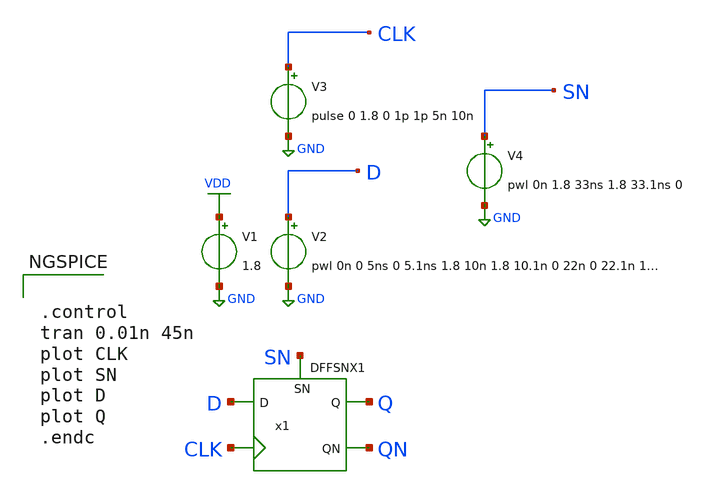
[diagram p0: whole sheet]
** sch_path: lib/xschem/test_DFFSNX1.sch
**.subckt test_DFFSNX1
V2 D GND pwl 0n 0 5ns 0 5.1ns 1.8 10n 1.8 10.1n 0 22n 0 22.1n 1.8 27n 1.8 27.1n 0 34n 0 34.1n 1.8
V1 VDD GND 1.8
V3 CLK GND pulse 0 1.8 0 1p 1p 5n 10n
V4 SN GND pwl 0n 1.8 33ns 1.8 33.1ns 0
x1 Q QN D CLK SN VDD GND DFFSNX1
**** begin user architecture code

.lib $::SKYWATER_MODELS/sky130.lib.spice tt


**** end user architecture code
**.ends

* expanding   symbol:  DFFSNX1.sym # of pins=5
** sym_path: DFFSNX1.sym
** sch_path: DFFSNX1.sch
.subckt DFFSNX1 Q QN D CLK SN VDD VSS
*.ipin D
*.opin QN
*.ipin SN
*.ipin CLK
*.opin Q
x1 net3 net1 SN net4 VDD VSS NAND3X1
x2 net4 net3 CLK VDD VSS NAND2X1
x3 net2 net1 CLK net4 VDD VSS NAND3X1
x4 net1 D net2 VDD VSS NAND2X1
x5 QN net2 Q VDD VSS NAND2X1
x6 Q QN SN net4 VDD VSS NAND3X1
.ends


* expanding   symbol:  NAND3X1.sym # of pins=4
** sym_path: lib/xschem/NAND3X1.sym
** sch_path: lib/xschem/NAND3X1.sch
.subckt NAND3X1 Y A B C VDD VSS
*.ipin A
*.opin Y
*.ipin B
*.ipin C
XM1 net2 C VSS VSS sky130_fd_pr__nfet_01v8 L=0.15 W=3 nf=1 ad='int((nf+1)/2) * W/nf * 0.29' as='int((nf+2)/2) * W/nf * 0.29'
+ pd='2*int((nf+1)/2) * (W/nf + 0.29)' ps='2*int((nf+2)/2) * (W/nf + 0.29)' nrd='0.29 / W' nrs='0.29 / W'
+ sa=0 sb=0 sd=0 mult=1 m=1
XM2 Y A VDD VDD sky130_fd_pr__pfet_01v8 L=0.15 W=2 nf=1 ad='int((nf+1)/2) * W/nf * 0.29' as='int((nf+2)/2) * W/nf * 0.29'
+ pd='2*int((nf+1)/2) * (W/nf + 0.29)' ps='2*int((nf+2)/2) * (W/nf + 0.29)' nrd='0.29 / W' nrs='0.29 / W'
+ sa=0 sb=0 sd=0 mult=1 m=1
XM3 net1 B net2 VSS sky130_fd_pr__nfet_01v8 L=0.15 W=3 nf=1 ad='int((nf+1)/2) * W/nf * 0.29' as='int((nf+2)/2) * W/nf * 0.29'
+ pd='2*int((nf+1)/2) * (W/nf + 0.29)' ps='2*int((nf+2)/2) * (W/nf + 0.29)' nrd='0.29 / W' nrs='0.29 / W'
+ sa=0 sb=0 sd=0 mult=1 m=1
XM4 Y A net1 VSS sky130_fd_pr__nfet_01v8 L=0.15 W=3 nf=1 ad='int((nf+1)/2) * W/nf * 0.29' as='int((nf+2)/2) * W/nf * 0.29'
+ pd='2*int((nf+1)/2) * (W/nf + 0.29)' ps='2*int((nf+2)/2) * (W/nf + 0.29)' nrd='0.29 / W' nrs='0.29 / W'
+ sa=0 sb=0 sd=0 mult=1 m=1
XM5 Y A VDD VDD sky130_fd_pr__pfet_01v8 L=0.15 W=2 nf=1 ad='int((nf+1)/2) * W/nf * 0.29' as='int((nf+2)/2) * W/nf * 0.29'
+ pd='2*int((nf+1)/2) * (W/nf + 0.29)' ps='2*int((nf+2)/2) * (W/nf + 0.29)' nrd='0.29 / W' nrs='0.29 / W'
+ sa=0 sb=0 sd=0 mult=1 m=1
XM6 Y B VDD VDD sky130_fd_pr__pfet_01v8 L=0.15 W=2 nf=1 ad='int((nf+1)/2) * W/nf * 0.29' as='int((nf+2)/2) * W/nf * 0.29'
+ pd='2*int((nf+1)/2) * (W/nf + 0.29)' ps='2*int((nf+2)/2) * (W/nf + 0.29)' nrd='0.29 / W' nrs='0.29 / W'
+ sa=0 sb=0 sd=0 mult=1 m=1
XM7 Y B VDD VDD sky130_fd_pr__pfet_01v8 L=0.15 W=2 nf=1 ad='int((nf+1)/2) * W/nf * 0.29' as='int((nf+2)/2) * W/nf * 0.29'
+ pd='2*int((nf+1)/2) * (W/nf + 0.29)' ps='2*int((nf+2)/2) * (W/nf + 0.29)' nrd='0.29 / W' nrs='0.29 / W'
+ sa=0 sb=0 sd=0 mult=1 m=1
XM8 Y C VDD VDD sky130_fd_pr__pfet_01v8 L=0.15 W=2 nf=1 ad='int((nf+1)/2) * W/nf * 0.29' as='int((nf+2)/2) * W/nf * 0.29'
+ pd='2*int((nf+1)/2) * (W/nf + 0.29)' ps='2*int((nf+2)/2) * (W/nf + 0.29)' nrd='0.29 / W' nrs='0.29 / W'
+ sa=0 sb=0 sd=0 mult=1 m=1
XM9 Y C VDD VDD sky130_fd_pr__pfet_01v8 L=0.15 W=2 nf=1 ad='int((nf+1)/2) * W/nf * 0.29' as='int((nf+2)/2) * W/nf * 0.29'
+ pd='2*int((nf+1)/2) * (W/nf + 0.29)' ps='2*int((nf+2)/2) * (W/nf + 0.29)' nrd='0.29 / W' nrs='0.29 / W'
+ sa=0 sb=0 sd=0 mult=1 m=1
.ends


* expanding   symbol:  NAND2X1.sym # of pins=3
** sym_path: lib/xschem/NAND2X1.sym
** sch_path: lib/xschem/NAND2X1.sch
.subckt NAND2X1 Y A B VDD VSS
*.ipin A
*.opin Y
*.ipin B
XM1 Y A VDD VDD sky130_fd_pr__pfet_01v8 L=0.15 W=2 nf=1 ad='int((nf+1)/2) * W/nf * 0.29' as='int((nf+2)/2) * W/nf * 0.29'
+ pd='2*int((nf+1)/2) * (W/nf + 0.29)' ps='2*int((nf+2)/2) * (W/nf + 0.29)' nrd='0.29 / W' nrs='0.29 / W'
+ sa=0 sb=0 sd=0 mult=1 m=1
XM5 Y A net1 VSS sky130_fd_pr__nfet_01v8 L=0.15 W=3 nf=1 ad='int((nf+1)/2) * W/nf * 0.29' as='int((nf+2)/2) * W/nf * 0.29'
+ pd='2*int((nf+1)/2) * (W/nf + 0.29)' ps='2*int((nf+2)/2) * (W/nf + 0.29)' nrd='0.29 / W' nrs='0.29 / W'
+ sa=0 sb=0 sd=0 mult=1 m=1
XM2 Y A VDD VDD sky130_fd_pr__pfet_01v8 L=0.15 W=2 nf=1 ad='int((nf+1)/2) * W/nf * 0.29' as='int((nf+2)/2) * W/nf * 0.29'
+ pd='2*int((nf+1)/2) * (W/nf + 0.29)' ps='2*int((nf+2)/2) * (W/nf + 0.29)' nrd='0.29 / W' nrs='0.29 / W'
+ sa=0 sb=0 sd=0 mult=1 m=1
XM3 Y B VDD VDD sky130_fd_pr__pfet_01v8 L=0.15 W=2 nf=1 ad='int((nf+1)/2) * W/nf * 0.29' as='int((nf+2)/2) * W/nf * 0.29'
+ pd='2*int((nf+1)/2) * (W/nf + 0.29)' ps='2*int((nf+2)/2) * (W/nf + 0.29)' nrd='0.29 / W' nrs='0.29 / W'
+ sa=0 sb=0 sd=0 mult=1 m=1
XM4 Y B VDD VDD sky130_fd_pr__pfet_01v8 L=0.15 W=2 nf=1 ad='int((nf+1)/2) * W/nf * 0.29' as='int((nf+2)/2) * W/nf * 0.29'
+ pd='2*int((nf+1)/2) * (W/nf + 0.29)' ps='2*int((nf+2)/2) * (W/nf + 0.29)' nrd='0.29 / W' nrs='0.29 / W'
+ sa=0 sb=0 sd=0 mult=1 m=1
XM6 net1 B VSS VSS sky130_fd_pr__nfet_01v8 L=0.15 W=3 nf=1 ad='int((nf+1)/2) * W/nf * 0.29' as='int((nf+2)/2) * W/nf * 0.29'
+ pd='2*int((nf+1)/2) * (W/nf + 0.29)' ps='2*int((nf+2)/2) * (W/nf + 0.29)' nrd='0.29 / W' nrs='0.29 / W'
+ sa=0 sb=0 sd=0 mult=1 m=1
.ends

.GLOBAL VDD
.GLOBAL GND
**** begin user architecture code


.control
tran 0.01n 45n
plot CLK
plot SN
plot D
plot Q
.endc


**** end user architecture code
.end
